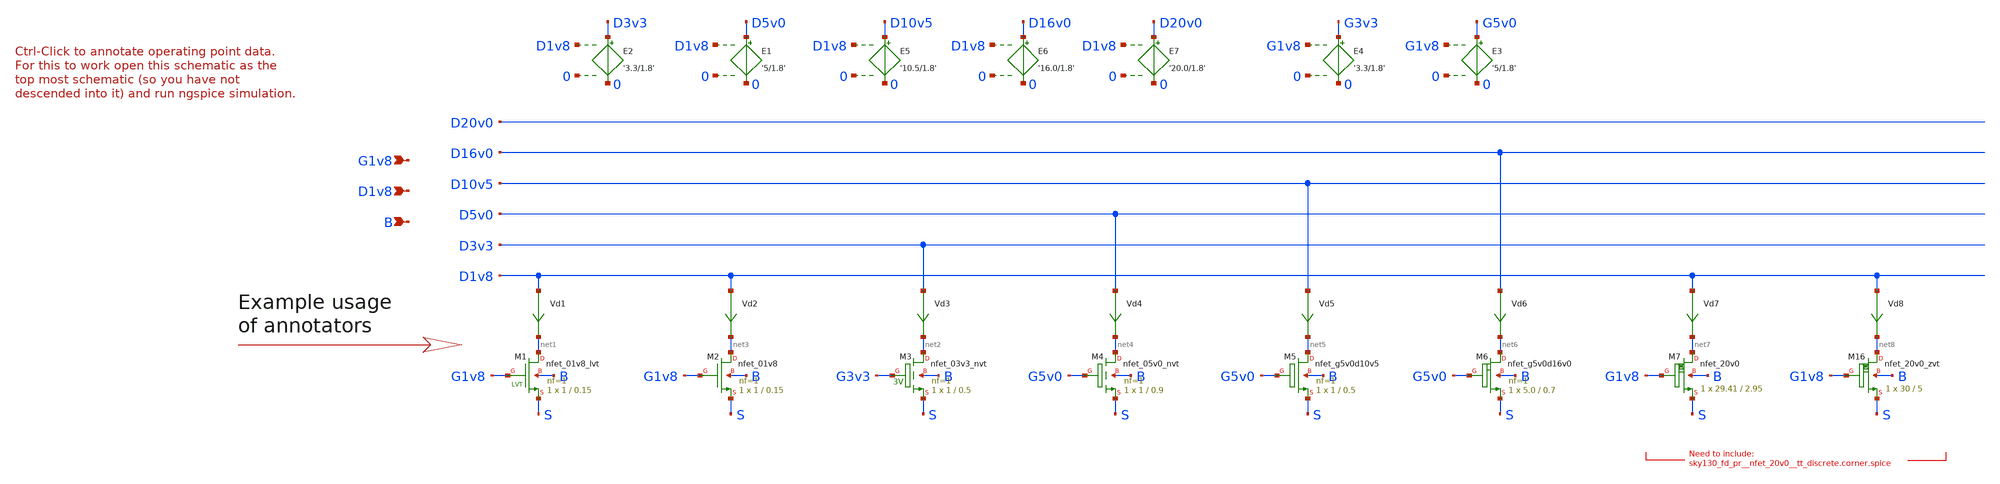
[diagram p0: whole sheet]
** sch_path: pdks/sky130A-1.0.227.01/libs.tech/xschem/sky130_tests/test_nmos.sch
* Copyright 2021 Stefan Frederik Schippers
* Licensed under the Apache License, Version 2.0 (the "License");
* you may not use this file except in compliance with the License.
* You may obtain a copy of the License at
* https://www.apache.org/licenses/LICENSE-2.0
* Unless required by applicable law or agreed to in writing, software
* distributed under the License is distributed on an "AS IS" BASIS,
* WITHOUT WARRANTIES OR CONDITIONS OF ANY KIND, either express or implied.
* See the License for the specific language governing permissions and
* limitations under the License.
**.subckt test_nmos G1v8 D1v8 B
*.ipin G1v8
*.ipin D1v8
*.ipin B
Vd1 D1v8 net1 0
.save i(vd1)
Vd3 D3v3 net2 0
.save i(vd3)
Vd2 D1v8 net3 0
.save i(vd2)
Vd4 D5v0 net4 0
.save i(vd4)
E1 D5v0 0 D1v8 0 '5/1.8'
E2 D3v3 0 D1v8 0 '3.3/1.8'
E3 G5v0 0 G1v8 0 '5/1.8'
E4 G3v3 0 G1v8 0 '3.3/1.8'
Vd5 D10v5 net5 0
.save i(vd5)
E5 D10v5 0 D1v8 0 '10.5/1.8'
E6 D16v0 0 D1v8 0 '16.0/1.8'
Vd6 D16v0 net6 0
.save i(vd6)
Vd7 D1v8 net7 0
.save i(vd7)
E7 D20v0 0 D1v8 0 '20.0/1.8'
XM1 net1 G1v8 S B sky130_fd_pr__nfet_01v8_lvt L=0.15 W=1 nf=1 ad='int((1 + 1)/2) * 1 / 1 * 0.29' as='int((1 + 2)/2) * 1 / 1 * 0.29'
+ pd='2*int((1 + 1)/2) * (1 / 1 + 0.29)' ps='2*int((1 + 2)/2) * (1 / 1 + 0.29)' nrd='0.29 / 1 ' nrs='0.29 / 1 '
+ sa=0 sb=0 sd=0 mult=1 m=1
XM2 net3 G1v8 S B sky130_fd_pr__nfet_01v8 L=0.15 W=1 nf=1 ad='int((1 + 1)/2) * 1 / 1 * 0.29' as='int((1 + 2)/2) * 1 / 1 * 0.29'
+ pd='2*int((1 + 1)/2) * (1 / 1 + 0.29)' ps='2*int((1 + 2)/2) * (1 / 1 + 0.29)' nrd='0.29 / 1 ' nrs='0.29 / 1 '
+ sa=0 sb=0 sd=0 mult=1 m=1
XM3 net2 G3v3 S B sky130_fd_pr__nfet_03v3_nvt L=0.5 W=1 nf=1 ad='int((1 + 1)/2) * 1 / 1 * 0.29' as='int((1 + 2)/2) * 1 / 1 * 0.29'
+ pd='2*int((1 + 1)/2) * (1 / 1 + 0.29)' ps='2*int((1 + 2)/2) * (1 / 1 + 0.29)' nrd='0.29 / 1 ' nrs='0.29 / 1 '
+ sa=0 sb=0 sd=0 mult=1 m=1
XM4 net4 G5v0 S B sky130_fd_pr__nfet_05v0_nvt L=0.9 W=1 nf=1 ad='int((1 + 1)/2) * 1 / 1 * 0.29' as='int((1 + 2)/2) * 1 / 1 * 0.29'
+ pd='2*int((1 + 1)/2) * (1 / 1 + 0.29)' ps='2*int((1 + 2)/2) * (1 / 1 + 0.29)' nrd='0.29 / 1 ' nrs='0.29 / 1 '
+ sa=0 sb=0 sd=0 mult=1 m=1
XM5 net5 G5v0 S B sky130_fd_pr__nfet_g5v0d10v5 L=0.5 W=1 nf=1 ad='int((1 + 1)/2) * 1 / 1 * 0.29' as='int((1 + 2)/2) * 1 / 1 * 0.29'
+ pd='2*int((1 + 1)/2) * (1 / 1 + 0.29)' ps='2*int((1 + 2)/2) * (1 / 1 + 0.29)' nrd='0.29 / 1 ' nrs='0.29 / 1 '
+ sa=0 sb=0 sd=0 mult=1 m=1
XM6 net6 G5v0 S B sky130_fd_pr__nfet_g5v0d16v0 L=0.7 W=5.0 nf=1 ad='int((nf+1)/2) * W/nf * 0.29' as='int((nf+2)/2) * W/nf * 0.29'
+ pd='2*int((nf+1)/2) * (W/nf + 0.29)' ps='2*int((nf+2)/2) * (W/nf + 0.29)' nrd='0.29 / W' nrs='0.29 / W'
+ sa=0 sb=0 sd=0 mult=1 m=1
Vd8 D1v8 net8 0
.save i(vd8)
XM7 net7 G1v8 S B sky130_fd_pr__nfet_20v0 L=2.95 W=29.41 m=1
XM16 net8 G1v8 S B sky130_fd_pr__nfet_20v0_zvt W=30 L=5 m=1
**** begin user architecture code

* this experimental option enables mos model bin
* selection based on W/NF instead of W
.option wnflag=1
.option savecurrents
vg G1v8 0 1.8
vs s 0 0
vd D1v8 0 1.8
vb b 0 0
.control
save all
dc vd 0 1.8 0.01 vg 0 1.8 0.2
* dc vd 0 1.8 0.01 vg 0 1.2 0.1
plot all.vd1#branch vs D1v8
*plot all.vd2#branch vs D1v8
plot all.vd3#branch vs D3v3
*plot all.vd4#branch vs D5v0
plot all.vd5#branch vs D10v5
*plot all.vd6#branch vs D16v0
plot all.vd8#branch vs D1v8
plot all.vd7#branch vs D1v8
save @m.xm1.msky130_fd_pr__nfet_01v8_lvt[gm]
op
write test_nmos.raw
.endc



** manual skywater-pdk install (with patches applied).

** opencircuitdesign pdks install

 ** manual skywater pdks install (with patches applied)
* .lib $::SKYWATER_MODELS/models/sky130.lib.spice tt

** opencircuitdesign pdks install
.lib $::SKYWATER_MODELS/sky130.lib.spice tt

.param mc_mm_switch=0
.param mc_pr_switch=0

**** end user architecture code
**.ends
.end
